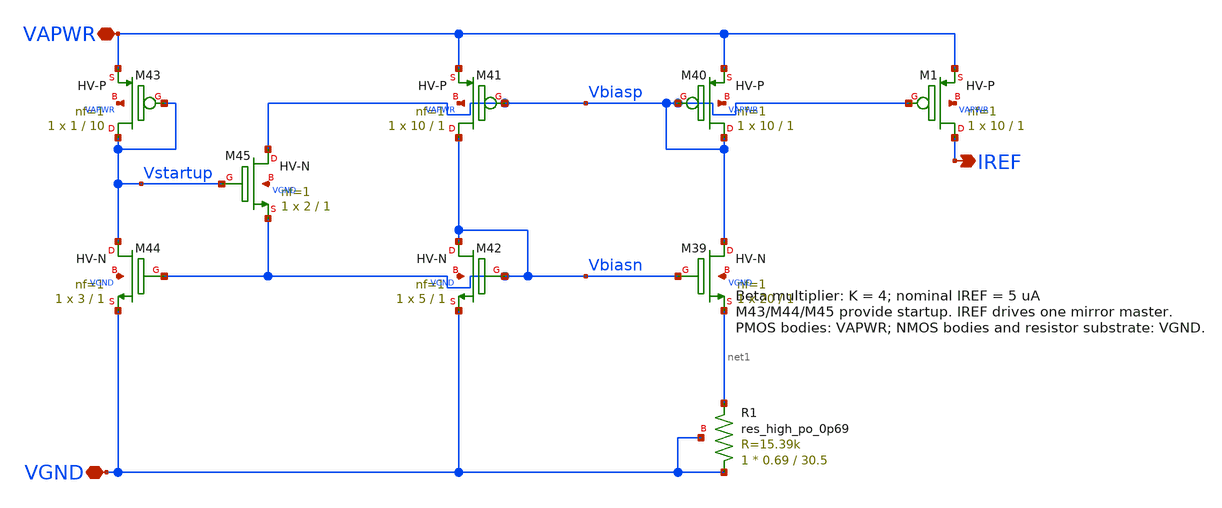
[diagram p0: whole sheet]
** sch_path: xschem/reference_bias_3v3.sch
**.subckt reference_bias_3v3 VAPWR VGND IREF
*.iopin VAPWR
*.iopin VGND
*.opin IREF
XR1 VGND net1 VGND sky130_fd_pr__res_high_po_0p69 L=30.5 mult=1 m=1
XM40 Vbiasp Vbiasp VAPWR VAPWR sky130_fd_pr__pfet_g5v0d10v5 L=1 W=10 nf=1 ad='int((nf+1)/2) * W/nf * 0.29'
+ as='int((nf+2)/2) * W/nf * 0.29' pd='2*int((nf+1)/2) * (W/nf + 0.29)' ps='2*int((nf+2)/2) * (W/nf + 0.29)'
+ nrd='0.29 / W' nrs='0.29 / W' sa=0 sb=0 sd=0 mult=1 m=1
XM44 Vstartup Vbiasn VGND VGND sky130_fd_pr__nfet_g5v0d10v5 L=1 W=3 nf=1 ad='int((nf+1)/2) * W/nf * 0.29'
+ as='int((nf+2)/2) * W/nf * 0.29' pd='2*int((nf+1)/2) * (W/nf + 0.29)' ps='2*int((nf+2)/2) * (W/nf + 0.29)'
+ nrd='0.29 / W' nrs='0.29 / W' sa=0 sb=0 sd=0 mult=1 m=1
XM41 Vbiasn Vbiasp VAPWR VAPWR sky130_fd_pr__pfet_g5v0d10v5 L=1 W=10 nf=1 ad='int((nf+1)/2) * W/nf * 0.29'
+ as='int((nf+2)/2) * W/nf * 0.29' pd='2*int((nf+1)/2) * (W/nf + 0.29)' ps='2*int((nf+2)/2) * (W/nf + 0.29)'
+ nrd='0.29 / W' nrs='0.29 / W' sa=0 sb=0 sd=0 mult=1 m=1
XM43 Vstartup Vstartup VAPWR VAPWR sky130_fd_pr__pfet_g5v0d10v5 L=10 W=1 nf=1 ad='int((nf+1)/2) * W/nf * 0.29'
+ as='int((nf+2)/2) * W/nf * 0.29' pd='2*int((nf+1)/2) * (W/nf + 0.29)' ps='2*int((nf+2)/2) * (W/nf + 0.29)'
+ nrd='0.29 / W' nrs='0.29 / W' sa=0 sb=0 sd=0 mult=1 m=1
XM42 Vbiasn Vbiasn VGND VGND sky130_fd_pr__nfet_g5v0d10v5 L=1 W=5 nf=1 ad='int((nf+1)/2) * W/nf * 0.29'
+ as='int((nf+2)/2) * W/nf * 0.29' pd='2*int((nf+1)/2) * (W/nf + 0.29)' ps='2*int((nf+2)/2) * (W/nf + 0.29)'
+ nrd='0.29 / W' nrs='0.29 / W' sa=0 sb=0 sd=0 mult=1 m=1
XM39 Vbiasp Vbiasn net1 VGND sky130_fd_pr__nfet_g5v0d10v5 L=1 W=20 nf=1 ad='int((nf+1)/2) * W/nf * 0.29'
+ as='int((nf+2)/2) * W/nf * 0.29' pd='2*int((nf+1)/2) * (W/nf + 0.29)' ps='2*int((nf+2)/2) * (W/nf + 0.29)'
+ nrd='0.29 / W' nrs='0.29 / W' sa=0 sb=0 sd=0 mult=1 m=1
XM45 Vbiasp Vstartup Vbiasn VGND sky130_fd_pr__nfet_g5v0d10v5 L=1 W=2 nf=1 ad='int((nf+1)/2) * W/nf * 0.29'
+ as='int((nf+2)/2) * W/nf * 0.29' pd='2*int((nf+1)/2) * (W/nf + 0.29)' ps='2*int((nf+2)/2) * (W/nf + 0.29)'
+ nrd='0.29 / W' nrs='0.29 / W' sa=0 sb=0 sd=0 mult=1 m=1
XM1 IREF Vbiasp VAPWR VAPWR sky130_fd_pr__pfet_g5v0d10v5 L=1 W=10 nf=1 ad='int((nf+1)/2) * W/nf * 0.29'
+ as='int((nf+2)/2) * W/nf * 0.29' pd='2*int((nf+1)/2) * (W/nf + 0.29)' ps='2*int((nf+2)/2) * (W/nf + 0.29)'
+ nrd='0.29 / W' nrs='0.29 / W' sa=0 sb=0 sd=0 mult=1 m=1
**.ends
.end
